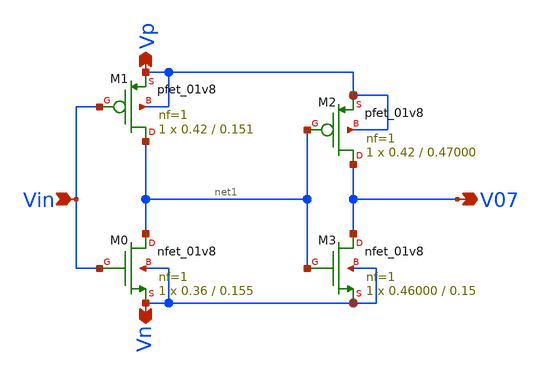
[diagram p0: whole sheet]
** sch_path: xschem/Vth_sch/Symbol/th07_backup.sch
**.subckt th07_backup Vn Vp Vin V07
*.opin Vn
*.opin Vp
*.ipin Vin
*.opin V07
XM2 V07 net1 Vp Vp sky130_fd_pr__pfet_01v8 L=0.47000 W=0.42 nf=1 ad='int((nf+1)/2) * W/nf * 0.29' as='int((nf+2)/2) * W/nf * 0.29'
+ pd='2*int((nf+1)/2) * (W/nf + 0.29)' ps='2*int((nf+2)/2) * (W/nf + 0.29)' nrd='0.29 / W' nrs='0.29 / W'
+ sa=0 sb=0 sd=0 mult=1 m=1
XM3 V07 net1 Vn Vn sky130_fd_pr__nfet_01v8 L=0.15 W=0.46000 nf=1 ad='int((nf+1)/2) * W/nf * 0.29' as='int((nf+2)/2) * W/nf * 0.29'
+ pd='2*int((nf+1)/2) * (W/nf + 0.29)' ps='2*int((nf+2)/2) * (W/nf + 0.29)' nrd='0.29 / W' nrs='0.29 / W'
+ sa=0 sb=0 sd=0 mult=1 m=1
XM1 net1 Vin Vp Vp sky130_fd_pr__pfet_01v8 L=0.151 W=0.42 nf=1 ad='int((nf+1)/2) * W/nf * 0.29' as='int((nf+2)/2) * W/nf * 0.29'
+ pd='2*int((nf+1)/2) * (W/nf + 0.29)' ps='2*int((nf+2)/2) * (W/nf + 0.29)' nrd='0.29 / W' nrs='0.29 / W'
+ sa=0 sb=0 sd=0 mult=1 m=1
XM0 net1 Vin Vn Vn sky130_fd_pr__nfet_01v8 L=0.155 W=0.36 nf=1 ad='int((nf+1)/2) * W/nf * 0.29' as='int((nf+2)/2) * W/nf * 0.29'
+ pd='2*int((nf+1)/2) * (W/nf + 0.29)' ps='2*int((nf+2)/2) * (W/nf + 0.29)' nrd='0.29 / W' nrs='0.29 / W'
+ sa=0 sb=0 sd=0 mult=1 m=1
**.ends
.end
